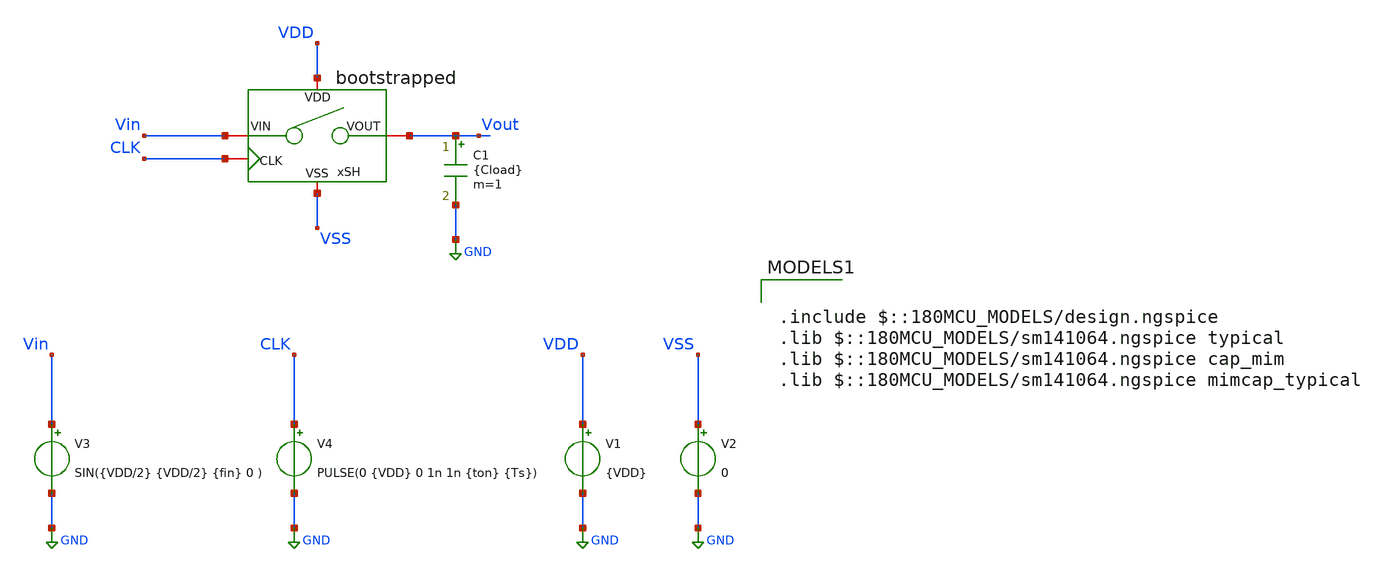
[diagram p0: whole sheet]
** sch_path: designs/sar_adc/samplehold/bootstrapped/xschem/tb_bootstrapped.sch
**.subckt tb_bootstrapped
V1 VDD GND {VDD}
V2 VSS GND 0
V3 Vin GND SIN({VDD/2} {VDD/2} {fin} 0 )
V4 CLK GND PULSE(0 {VDD} 0 1n 1n {ton} {Ts})
C1 Vout GND {Cload} m=1
xSH VDD VSS CLK Vin Vout bootstrapped
**** begin user architecture code

.include $::180MCU_MODELS/design.ngspice
.lib $::180MCU_MODELS/sm141064.ngspice typical
.lib $::180MCU_MODELS/sm141064.ngspice cap_mim
.lib $::180MCU_MODELS/sm141064.ngspice mimcap_typical





* Sampling clock
.param Fs = 5Meg
.param ton = Ts/12

* Input parameters
.param Ts = 1/Fs
.param Ns = 1024
.param Nc = 103
.param fin = Nc/Ns*Fs

* Test-bench parameters
.temp 27
.param VDD = 3.3
.param Cload = 1p

.save all

.control

* Local variables for .control
let Fs = 5Meg
let Ns = 1024
let Nspare = 5

let tstep = 1/(Fs*250)
let tstop = (Ns + Nspare)/Fs

* Transient simulation
tran $&tstep $&tstop
*power
let IDD=-1*i(v1)

meas tran I_avg AVG IDD from=tstep to=tstop
meas tran v_avg AVG v(vdd) from=tstep to=tstop
let P_avg = abs(I_avg*v_avg)
print P_avg

linearize v(vout) v(vin) v(clk)
wrdata tb_bootstrapped.csv v(vin) v(vout) v(clk)

plot v(vin) v(vout)
plot v(vin) v(vout) xl 0 4u

.endc



**** end user architecture code
**.ends
.GLOBAL GND
.end
